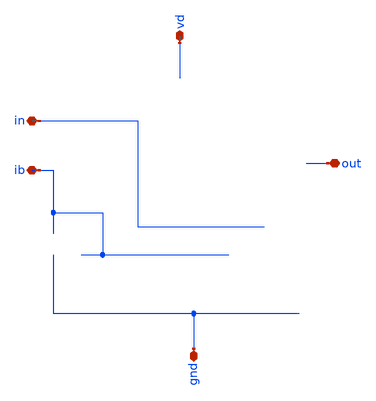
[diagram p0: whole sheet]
** sch_path: buffer/xschem/buffer-pex.sch
* Copyright 2020 Stefan Frederik Schippers
* Licensed under the Apache License, Version 2.0 (the "License");
* you may not use this file except in compliance with the License.
* You may obtain a copy of the License at
* https://www.apache.org/licenses/LICENSE-2.0
* Unless required by applicable law or agreed to in writing, software
* distributed under the License is distributed on an "AS IS" BASIS,
* WITHOUT WARRANTIES OR CONDITIONS OF ANY KIND, either express or implied.
* See the License for the specific language governing permissions and
* limitations under the License.
**.subckt buffer-pex vd ib out in gnd
*.iopin vd
*.iopin ib
*.iopin out
*.iopin in
*.iopin gnd
**** begin user architecture code


* NGSPICE file created from buffer.ext - technology: sky130A

*.subckt buffer vd ib out in gnd
X0 b.t12 b.t11 vd.t18 vd.t17 sky130_fd_pr__pfet_01v8 ad=0.145 pd=1.29 as=0.145 ps=1.29 w=1 l=1
X1 vd.t25 vd.t22 vd.t24 vd.t23 sky130_fd_pr__pfet_01v8 ad=0.29 pd=2.58 as=0 ps=0 w=1 l=1
X2 c out a gnd.t2 sky130_fd_pr__nfet_01v8 ad=0.248 pd=1.83 as=0.248 ps=1.83 w=1.5 l=0.15
X3 out.t7 d.t12 gnd.t6 gnd.t5 sky130_fd_pr__nfet_01v8 ad=0.725 pd=5.29 as=0.725 ps=5.29 w=5 l=1
X4 a a a vd.t41 sky130_fd_pr__pfet_01v8 ad=0.145 pd=1.29 as=1.16 ps=10.3 w=1 l=1
X5 d.t11 a vd.t40 vd.t39 sky130_fd_pr__pfet_01v8 ad=2.17 pd=15.3 as=2.17 ps=15.3 w=15 l=1
X6 d.t5 d.t4 d.t5 vd.t42 sky130_fd_pr__pfet_01v8 ad=2.17 pd=15.3 as=0 ps=0 w=15 l=1
X7 vd.t21 vd.t19 vd.t21 vd.t20 sky130_fd_pr__pfet_01v8 ad=0.145 pd=1.29 as=0 ps=0 w=1 l=1
X8 a a vd.t38 vd.t37 sky130_fd_pr__pfet_01v8 ad=0.145 pd=1.29 as=0.145 ps=1.29 w=1 l=1
X9 gnd.t24 d.t13 out.t8 gnd.t23 sky130_fd_pr__nfet_01v8 ad=0.725 pd=5.29 as=0.725 ps=5.29 w=5 l=1
X10 vd.t16 b.t16 out.t6 vd.t15 sky130_fd_pr__pfet_01v8 ad=2.17 pd=15.3 as=2.17 ps=15.3 w=15 l=1
X11 out.t4 out.t2 out.t3 vd.t0 sky130_fd_pr__pfet_01v8 ad=4.35 pd=30.6 as=0 ps=0 w=15 l=1
X12 d.t9 d.t8 gnd.t9 gnd.t8 sky130_fd_pr__nfet_01v8 ad=0.725 pd=5.29 as=0.725 ps=5.29 w=5 l=1
X13 a a vd.t36 vd.t35 sky130_fd_pr__pfet_01v8 ad=0.145 pd=1.29 as=0.145 ps=1.29 w=1 l=1
X14 b.t6 b.t4 b.t5 vd.t14 sky130_fd_pr__pfet_01v8 ad=0.29 pd=2.58 as=0 ps=0 w=1 l=1
X15 a a a gnd.t13 sky130_fd_pr__nfet_01v8 ad=0.465 pd=3.62 as=0.96 ps=7.28 w=1.5 l=0.15
X16 gnd.t20 gnd.t17 gnd.t19 gnd.t18 sky130_fd_pr__nfet_01v8 ad=1.45 pd=10.6 as=0 ps=0 w=5 l=1
X17 vd.t34 a a vd.t33 sky130_fd_pr__pfet_01v8 ad=0.145 pd=1.29 as=0.145 ps=1.29 w=1 l=1
X18 vd.t32 a a vd.t31 sky130_fd_pr__pfet_01v8 ad=0.145 pd=1.29 as=0.145 ps=1.29 w=1 l=1
X19 a a vd.t30 vd.t29 sky130_fd_pr__pfet_01v8 ad=0.145 pd=1.29 as=0.145 ps=1.29 w=1 l=1
X20 b.t3 b.t2 b.t3 gnd.t4 sky130_fd_pr__nfet_01v8 ad=0.248 pd=1.83 as=0 ps=0 w=1.5 l=0.15
X21 gnd.t1 ib.t3 ib.t4 gnd.t0 sky130_fd_pr__nfet_01v8 ad=0.145 pd=1.29 as=0.145 ps=1.29 w=1 l=1
X22 c ib.t5 gnd.t11 gnd.t10 sky130_fd_pr__nfet_01v8 ad=0.145 pd=1.29 as=0.145 ps=1.29 w=1 l=1
X23 ib.t2 ib.t0 ib.t1 gnd.t7 sky130_fd_pr__nfet_01v8 ad=0.29 pd=2.58 as=0 ps=0 w=1 l=1
X24 out.t5 b.t17 vd.t13 vd.t12 sky130_fd_pr__pfet_01v8 ad=2.17 pd=15.3 as=2.17 ps=15.3 w=15 l=1
X25 b.t10 b.t9 vd vd.t9 sky130_fd_pr__pfet_01v8 ad=0.145 pd=1.29 as=0.145 ps=1.29 w=1 l=1
X26 vd b.t7 b.t8 vd.t6 sky130_fd_pr__pfet_01v8 ad=0.145 pd=1.29 as=0.145 ps=1.29 w=1 l=1
X27 gnd.t22 d.t6 d.t7 gnd.t21 sky130_fd_pr__nfet_01v8 ad=0.725 pd=5.29 as=0.725 ps=5.29 w=5 l=1
X28 out.t1 out.t0 out.t1 vd.t26 sky130_fd_pr__pfet_01v8 ad=2.17 pd=15.3 as=0 ps=0 w=15 l=1
X29 vd.t5 b.t13 b.t14 vd.t4 sky130_fd_pr__pfet_01v8 ad=0.145 pd=1.29 as=0.145 ps=1.29 w=1 l=1
X30 b.t15 in.t0 c gnd.t12 sky130_fd_pr__nfet_01v8 ad=0.248 pd=1.83 as=0.248 ps=1.83 w=1.5 l=0.15
X31 c c c gnd.t3 sky130_fd_pr__nfet_01v8 ad=0.145 pd=1.29 as=1.08 ps=8.82 w=1 l=1
X32 vd.t28 a d.t10 vd.t27 sky130_fd_pr__pfet_01v8 ad=2.17 pd=15.3 as=2.17 ps=15.3 w=15 l=1
X33 d.t3 d.t1 d.t2 vd.t1 sky130_fd_pr__pfet_01v8 ad=4.35 pd=30.6 as=0 ps=0 w=15 l=1
X34 out d.t0 sky130_fd_pr__cap_mim_m3_2 l=15 w=30
X35 vd.t3 b.t0 b.t1 vd.t2 sky130_fd_pr__pfet_01v8 ad=0.145 pd=1.29 as=0.145 ps=1.29 w=1 l=1
X36 gnd.t16 gnd.t14 gnd.t16 gnd.t15 sky130_fd_pr__nfet_01v8 ad=0.725 pd=5.29 as=0 ps=0 w=5 l=1
R0 b.n11 b.t17 377.466
R1 b.n11 b.t16 376.93
R2 b.n18 b.t2 313.991
R3 b.t0 b.n11 41.3792
R4 b.n12 b.t0 40.2104
R5 b.n0 b.t6 28.5954
R6 b.n7 b.t8 28.5655
R7 b.n7 b.t5 28.5655
R8 b.n2 b.t1 28.5655
R9 b.n2 b.t12 28.5655
R10 b.n3 b.t14 28.5655
R11 b.n3 b.t10 28.5655
R12 b.n0 b.t4 26.3004
R13 b.n15 b.t7 26.2652
R14 b.n14 b.t9 26.2652
R15 b.n13 b.t13 26.2652
R16 b.n12 b.t11 26.2652
R17 b.n8 b.n7 25.3202
R18 b.n17 b.t15 13.2053
R19 b.n17 b.t3 6.63265
R20 b.n4 b.n2 1.62544
R21 b.n5 b.n4 1.44539
R22 b.n13 b.n12 0.718158
R23 b.n14 b.n13 0.718158
R24 b.n15 b.n14 0.718158
R25 b b.n18 0.594255
R26 b.n0 b.n15 0.517171
R27 b b.n16 0.502062
R28 b.n6 b.n5 0.191757
R29 b.n1 b.n6 0.189496
R30 b.n1 b.n10 0.162765
R31 b.n4 b.n3 0.156686
R32 b.n1 b.n0 0.0877146
R33 b.n10 b.n9 0.0870593
R34 b.n18 b.n17 0.0678366
R35 b.n16 b.n1 0.0614375
R36 b.n1 b.n8 0.0511368
R37 vd.n49 vd.n48 647.907
R38 vd.n49 vd.n32 647.529
R39 vd.t20 vd.t2 331.216
R40 vd.t2 vd.t17 331.216
R41 vd.t9 vd.t4 331.216
R42 vd.t6 vd.t9 331.216
R43 vd.t14 vd.t6 331.216
R44 vd.t41 vd.t35 331.216
R45 vd.t35 vd.t33 331.216
R46 vd.t33 vd.t29 331.216
R47 vd.t37 vd.t31 331.216
R48 vd.t23 vd.t37 331.216
R49 vd.n36 vd.t41 228.514
R50 vd.n35 vd.t14 210.542
R51 vd.t42 vd.t39 70.1694
R52 vd.t27 vd.t1 70.1694
R53 vd.t12 vd.t26 70.0291
R54 vd.t0 vd.t15 70.0291
R55 vd.n45 vd.t42 68.5376
R56 vd.t1 vd.n39 63.6434
R57 vd.n29 vd.t0 63.5148
R58 vd.t26 vd.n23 62.9732
R59 vd.n10 vd.t19 39.5312
R60 vd.n2 vd.t22 39.5292
R61 vd.n36 vd.n35 38.514
R62 vd.n42 vd.t27 37.5327
R63 vd.n26 vd.t12 35.2862
R64 vd.t15 vd.n26 34.7434
R65 vd.t39 vd.n42 32.6372
R66 vd.n2 vd.t25 28.6459
R67 vd.n0 vd.t36 28.5655
R68 vd.n0 vd.t34 28.5655
R69 vd.n1 vd.t38 28.5655
R70 vd.n1 vd.t24 28.5655
R71 vd.n4 vd.t30 28.5655
R72 vd.n4 vd.t32 28.5655
R73 vd.n11 vd.t21 28.5655
R74 vd.n11 vd.t3 28.5655
R75 vd.n13 vd.t18 28.5655
R76 vd.n13 vd.t5 28.5655
R77 vd.n30 vd.n29 21.216
R78 vd.n31 vd.n30 16.7426
R79 vd.n46 vd.t23 16.3842
R80 vd.n46 vd.n45 16.211
R81 vd.n30 vd.t20 12.5482
R82 vd.n47 vd.n46 7.64222
R83 vd.n21 vd.n9 5.78879
R84 vd.n8 vd.n7 5.72509
R85 vd.n19 vd.n18 2.24963
R86 vd.n7 vd.t40 1.90483
R87 vd.n7 vd.t28 1.90483
R88 vd.n9 vd.t13 1.90483
R89 vd.n9 vd.t16 1.90483
R90 vd.n8 vd.n6 1.79965
R91 vd.n14 vd.n12 1.56925
R92 vd.n5 vd.n3 1.5417
R93 vd.n15 vd.n14 1.438
R94 vd.n6 vd.n5 1.38515
R95 vd.n6 vd.n0 0.77517
R96 vd.n12 vd.n10 0.686006
R97 vd.n50 vd.n21 0.503104
R98 vd vd.n8 0.497524
R99 vd.n21 vd.n20 0.365502
R100 vd.n14 vd.n13 0.157684
R101 vd.n5 vd.n4 0.156686
R102 vd.n18 vd.n15 0.103522
R103 vd.n3 vd.n2 0.0791768
R104 vd.n18 vd.n17 0.0597867
R105 vd.n20 vd.n19 0.05675
R106 vd.n3 vd.n1 0.0493677
R107 vd.n12 vd.n11 0.0461626
R108 vd.n17 vd.n16 0.024973
R109 vd vd.n50 0.0239375
R110 vd.n25 vd.n24 0.00431884
R111 vd.n26 vd.n25 0.00431884
R112 vd.n41 vd.n40 0.00425193
R113 vd.n42 vd.n41 0.00425193
R114 vd.n48 vd.n47 0.00389051
R115 vd.n32 vd.n31 0.00389051
R116 vd.n44 vd.n43 0.0021559
R117 vd.n45 vd.n44 0.0021559
R118 vd.n28 vd.n27 0.00213065
R119 vd.n29 vd.n28 0.00213065
R120 vd.n39 vd.n38 0.00181202
R121 vd.n23 vd.n22 0.00181202
R122 vd.n34 vd.n33 0.0017783
R123 vd.n35 vd.n34 0.0017783
R124 vd.n49 vd.n37 0.000827345
R125 vd.n37 vd.n36 0.000827345
R126 vd.n50 vd.n49 0.000504092
R127 out.n4 out.t2 377.192
R128 out.n1 out.t0 377.175
R129 out.n7 out.t4 5.53268
R130 out.n6 out.t8 3.4805
R131 out.n6 out.t7 3.4805
R132 out.n7 out.n6 2.35238
R133 out.n5 out.n4 2.02858
R134 out.n2 out.n1 2.00736
R135 out.n3 out.t6 1.90483
R136 out.n3 out.t3 1.90483
R137 out.n0 out.t1 1.90483
R138 out.n0 out.t5 1.90483
R139 out.n8 out.n7 0.80675
R140 out out.n8 0.783312
R141 out.n8 out.n2 0.182565
R142 out.n7 out.n5 0.182565
R143 out.n5 out.n3 0.00195207
R144 out.n2 out.n0 0.00195207
R145 gnd.n23 gnd.n20 560.566
R146 gnd.n32 gnd.n27 547.013
R147 gnd.t21 gnd.t8 412.351
R148 gnd.t3 gnd.t10 412.351
R149 gnd.n30 gnd.t0 399.565
R150 gnd.n35 gnd.n32 374.579
R151 gnd.n21 gnd.t15 348.421
R152 gnd.t13 gnd.t3 263.712
R153 gnd.n41 gnd.n40 242.918
R154 gnd.n24 gnd.t21 217.363
R155 gnd.t0 gnd.n29 214.167
R156 gnd.n24 gnd.t5 194.988
R157 gnd.t2 gnd.t13 153.434
R158 gnd.n41 gnd.n23 147.294
R159 gnd.n33 gnd.t2 107.084
R160 gnd.t18 gnd.t4 107.084
R161 gnd.n13 gnd.t17 65.675
R162 gnd.n6 gnd.t14 65.5414
R163 gnd.n21 gnd.t23 63.9308
R164 gnd.n38 gnd.t18 35.1621
R165 gnd.n44 gnd.n43 31.16
R166 gnd.n43 gnd.t11 17.4005
R167 gnd.n43 gnd.t1 17.4005
R168 gnd.n40 gnd.n35 13.5534
R169 gnd.n30 gnd.t7 12.7866
R170 gnd.n38 gnd.t12 11.1883
R171 gnd.n13 gnd.t20 6.44128
R172 gnd.n44 gnd.n42 6.30056
R173 gnd.n42 gnd.n18 4.9255
R174 gnd.n7 gnd.t16 3.4805
R175 gnd.n7 gnd.t24 3.4805
R176 gnd.n14 gnd.t9 3.4805
R177 gnd.n14 gnd.t19 3.4805
R178 gnd.n0 gnd.t6 3.4805
R179 gnd.n0 gnd.t22 3.4805
R180 gnd.n8 gnd.n6 3.21916
R181 gnd.n15 gnd.n13 2.95318
R182 gnd gnd.n44 1.74425
R183 gnd.n9 gnd.n8 0.618
R184 gnd.n16 gnd.n15 0.60175
R185 gnd.n11 gnd.n5 0.412265
R186 gnd.n18 gnd.n16 0.139389
R187 gnd.n18 gnd.n17 0.139389
R188 gnd.n5 gnd.n3 0.0593235
R189 gnd.n32 gnd.n31 0.0431634
R190 gnd.n31 gnd.n30 0.0431634
R191 gnd.n23 gnd.n22 0.0388129
R192 gnd.n22 gnd.n21 0.0388129
R193 gnd.n11 gnd.n2 0.0285795
R194 gnd.n35 gnd.n34 0.0215341
R195 gnd.n34 gnd.n33 0.0215341
R196 gnd.n16 gnd.n12 0.01925
R197 gnd.n40 gnd.n39 0.00984699
R198 gnd.n39 gnd.n38 0.00984699
R199 gnd.n27 gnd.n26 0.007537
R200 gnd.n20 gnd.n19 0.007537
R201 gnd.n29 gnd.n28 0.00701261
R202 gnd.n41 gnd.n25 0.00701261
R203 gnd.n25 gnd.n24 0.00701261
R204 gnd.n37 gnd.n36 0.00517349
R205 gnd.n38 gnd.n37 0.00517349
R206 gnd.n12 gnd.n11 0.00425
R207 gnd.n11 gnd.n10 0.00425
R208 gnd.n10 gnd.n9 0.003
R209 gnd.n8 gnd.n7 0.00294771
R210 gnd.n15 gnd.n14 0.00294771
R211 gnd.n5 gnd.n4 0.00278445
R212 gnd.n1 gnd.n0 0.00193715
R213 gnd.n2 gnd.n1 0.00100999
R214 gnd.n42 gnd.n41 0.000506305
R215 d.n9 d.t1 377.216
R216 d.n8 d.t4 377.163
R217 d.n2 d.t13 134.298
R218 d.n4 d.t8 133.787
R219 d.n3 d.t6 133.761
R220 d.n2 d.t12 133.761
R221 d.n0 d.t3 5.55126
R222 d.n6 d.t7 3.4805
R223 d.n6 d.t9 3.4805
R224 d d.n7 3.10062
R225 d.n0 d.n9 2.02586
R226 d.n1 d.n8 1.99422
R227 d.n5 d.t0 1.91167
R228 d.n1 d.t11 1.90534
R229 d.n0 d.t10 1.90483
R230 d.n0 d.t2 1.90483
R231 d.n1 d.t5 1.89094
R232 d d.n1 0.77675
R233 d.n1 d.n0 0.647901
R234 d.n3 d.n2 0.538
R235 d.n4 d.n3 0.394346
R236 d.n7 d.n6 0.151643
R237 d.n5 d.n4 0.0558728
R238 d.n7 d.n5 0.0333947
R239 ib.n0 ib.t5 38.0465
R240 ib.n0 ib.t3 37.3602
R241 ib.n1 ib.t0 18.7496
R242 ib.n1 ib.t2 17.4934
R243 ib.n8 ib.t4 17.4005
R244 ib.n8 ib.t1 17.4005
R245 ib ib.n12 5.82847
R246 ib.n8 ib.n7 1.98351
R247 ib.n9 ib.n6 1.5912
R248 ib.n12 ib.n0 0.27692
R249 ib.n4 ib.n1 0.097375
R250 ib.n3 ib.n2 0.0963763
R251 ib.n11 ib.n10 0.0208125
R252 ib.n12 ib.n11 0.0174603
R253 ib.n4 ib.n3 0.0127549
R254 ib.n10 ib.n9 0.00846233
R255 ib.n9 ib.n8 0.00846233
R256 ib.n5 ib.n4 0.0051875
R257 ib.n10 ib.n5 0.003625
R258 in in.t0 325.817
C0 a vd 5.21f
C1 d vd 3.92f
C2 vd ib 0.0124f
C3 c out 0.0405f
C4 c b 0.16f
C5 in a 0.227f
C6 d in 0.673f
C7 in ib 0.573f
C8 a out 0.0961f
C9 d out 35.6f
C10 a b 0.239f
C11 d b 0.0351f
C12 out ib 0.0478f
C13 c a 0.199f
C14 in vd 0.376f
C15 d c 0.0518f
C16 c ib 0.185f
C17 vd out 4.72f
C18 b vd 6.07f
C19 d a 1.27f
C20 a ib 0.00973f
C21 c vd 0.00332f
C22 in out 0.0539f
C23 d ib 0.468f
C24 in b 0.112f
C25 b out 1.93f
C26 in c 0.416f
*.ends



**** end user architecture code
**.ends
.end
